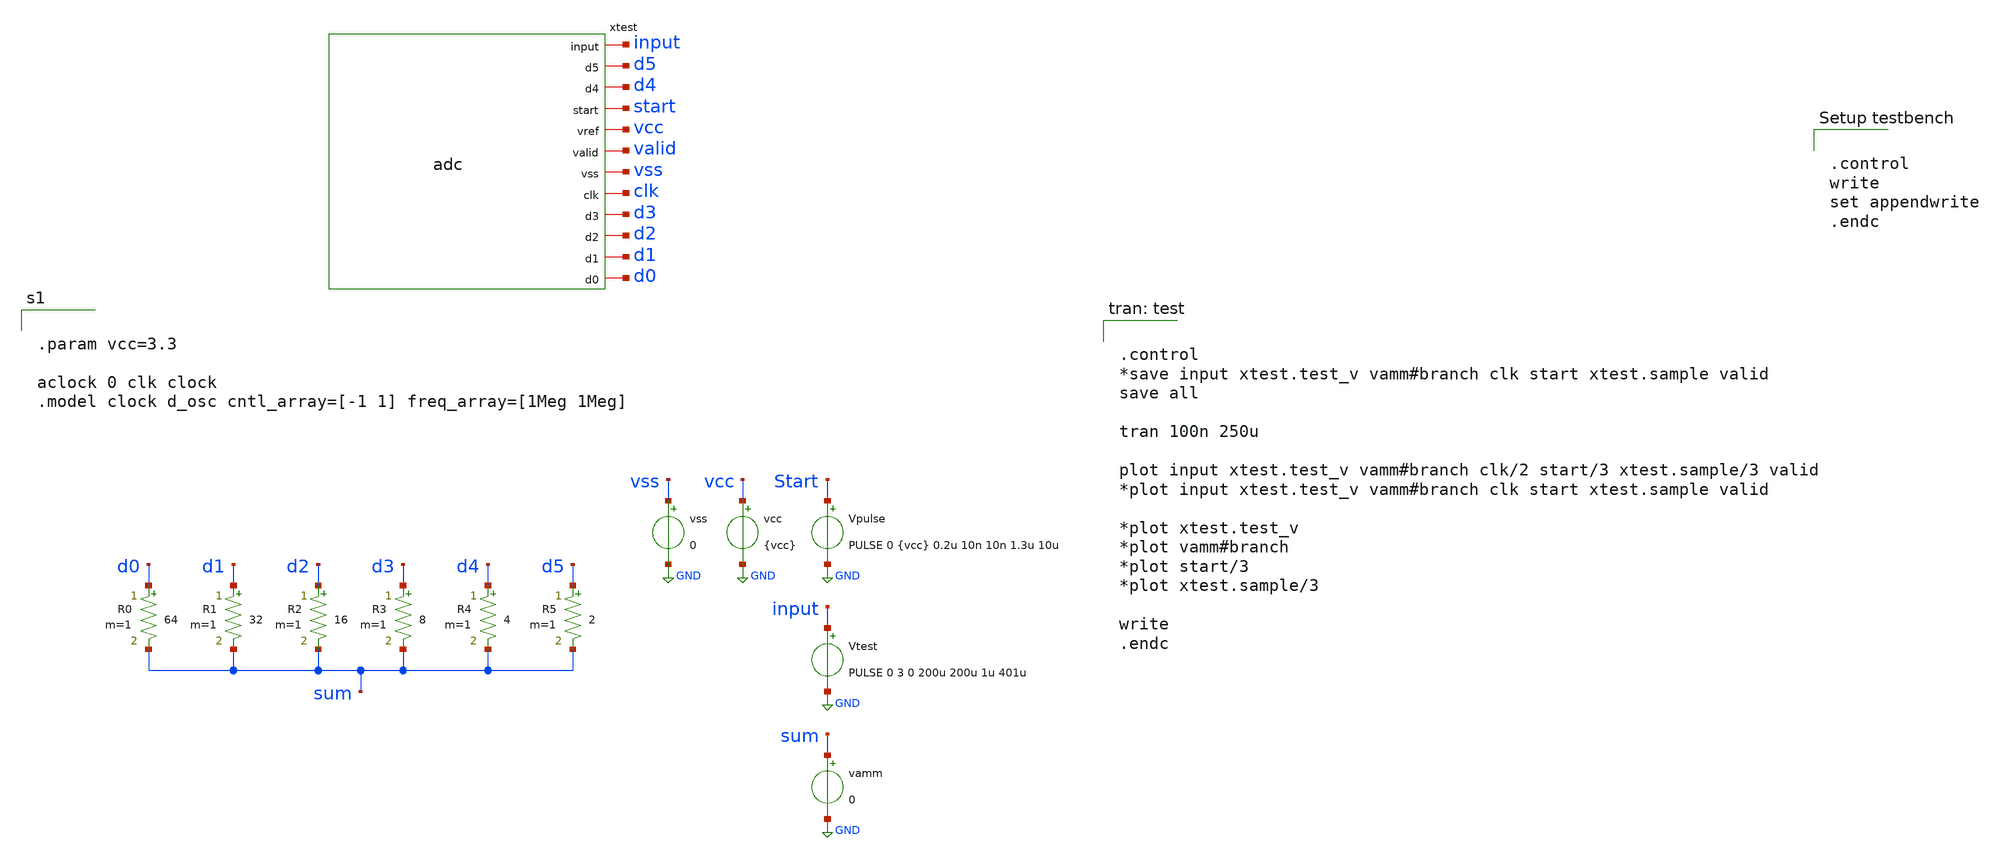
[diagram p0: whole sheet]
** sch_path: samples/digital_cosimulation/adc/test/adc_tb.sch

.control
write
set appendwrite
.endc


**.subckt adc_tb
vcc vcc GND {vcc}
Vpulse Start GND PULSE 0 {vcc} 0.2u 10n 10n 1.3u 10u
Vtest input GND PULSE 0 3 0 200u 200u 1u 401u
R1 d1 sum 32 m=1
R2 d2 sum 16 m=1
R3 d3 sum 8 m=1
R4 d4 sum 4 m=1
R5 d5 sum 2 m=1
R0 d0 sum 64 m=1
vamm sum GND 0
.save i(vamm)
xtest input d5 d4 start vcc valid vss clk d3 d2 d1 d0 adc
vss vss GND 0
**** begin user architecture code


.param vcc=3.3

aclock 0 clk clock
.model clock d_osc cntl_array=[-1 1] freq_array=[1Meg 1Meg]




.control
*save input xtest.test_v vamm#branch clk start xtest.sample valid
save all

tran 100n 250u

plot input xtest.test_v vamm#branch clk/2 start/3 xtest.sample/3 valid
*plot input xtest.test_v vamm#branch clk start xtest.sample valid

*plot xtest.test_v
*plot vamm#branch
*plot start/3
*plot xtest.sample/3

write
.endc


**** end user architecture code
**.ends

* expanding   symbol:  symbol/adc.sym # of pins=12
** sym_path: samples/digital_cosimulation/adc/symbol/adc.sym
** sch_path: samples/digital_cosimulation/adc/symbol/adc.sch
.subckt adc input d5 d4 start vref valid vss clk d3 d2 d1 d0
*.iopin vss
*.iopin vref
*.iopin start
*.iopin valid
*.iopin d5
*.iopin d4
*.iopin d3
*.iopin d2
*.iopin d1
*.iopin clk
*.iopin d0
*.iopin input
rin iin test_v 1k m=1
**** begin user architecture code


* An XSPICE ADC bridge functions as a comparator.

acomp [%vd(test_v vref)] [comp] comparator
.model comparator adc_bridge in_low=0 in_high=0

* The digital portion of the circuit is specified in compiled Verilog.
* Outputs inverted to cancel the inverter in subcircuit ccap,
* and produce the correct numerical output value.

adut [ clk comp start] [sample valid ~d5 ~d4 ~d3 ~d2 ~d1 ~d0] null dut
.model dut d_cosim simulation=../../code_models/adc.so

xsample       input iin sample vref tgate
.subckt tgate a     b   ctl    vdd
switch        a     b   ctl    0   tg
.model tg sw vt=1.5 ron=2k
.ends


**** end user architecture code
xb5 test_v vref d5 vss ccap c=1p
xb4 test_v vref d4 vss ccap c={1p/2}
xb3 test_v vref d3 vss ccap c={1p/4}
xb2 test_v vref d2 vss ccap c={1p/8}
xb1 test_v vref d1 vss ccap c={1p/16}
xb0 test_v vref d0 vss ccap c={1p/32}
clast test_v vss {1p/32} m=1
.ends


* expanding   symbol:  symbol/ccap.sym # of pins=4
** sym_path: samples/digital_cosimulation/ccap/symbol/ccap.sym
** sch_path: samples/digital_cosimulation/ccap/symbol/ccap.sch
.subckt ccap in vcc ctl vss  c=1p
*.iopin ctl
*.iopin in
*.iopin vcc
*.iopin vss
xinv ctl tail vcc vss ainv
cb in tail {c} m=1
.ends


* expanding   symbol:  symbol/ainv.sym # of pins=4
** sym_path: samples/digital_cosimulation/ainv/symbol/ainv.sym
** sch_path: samples/digital_cosimulation/ainv/symbol/ainv.sch
.subckt ainv in out vdd vss
*.iopin vdd
*.iopin out
*.iopin vss
*.iopin in
**** begin user architecture code


.model p1 pmos   level=2 vto=-0.5 kp=8.5e-6 gamma=0.4 phi=0.65 lambda=0.05 xj=0.5e-6
.model n1 nmos   level=2 vto=0.5 kp=24e-6 gamma=0.15 phi=0.65 lambda=0.015 xj=0.5e-6


**** end user architecture code
mn out in vss vss n1 w=5u l=0.18u m=1
mp out in vdd vdd p1 w=5u l=0.18u m=1
.ends

.GLOBAL GND
.end
